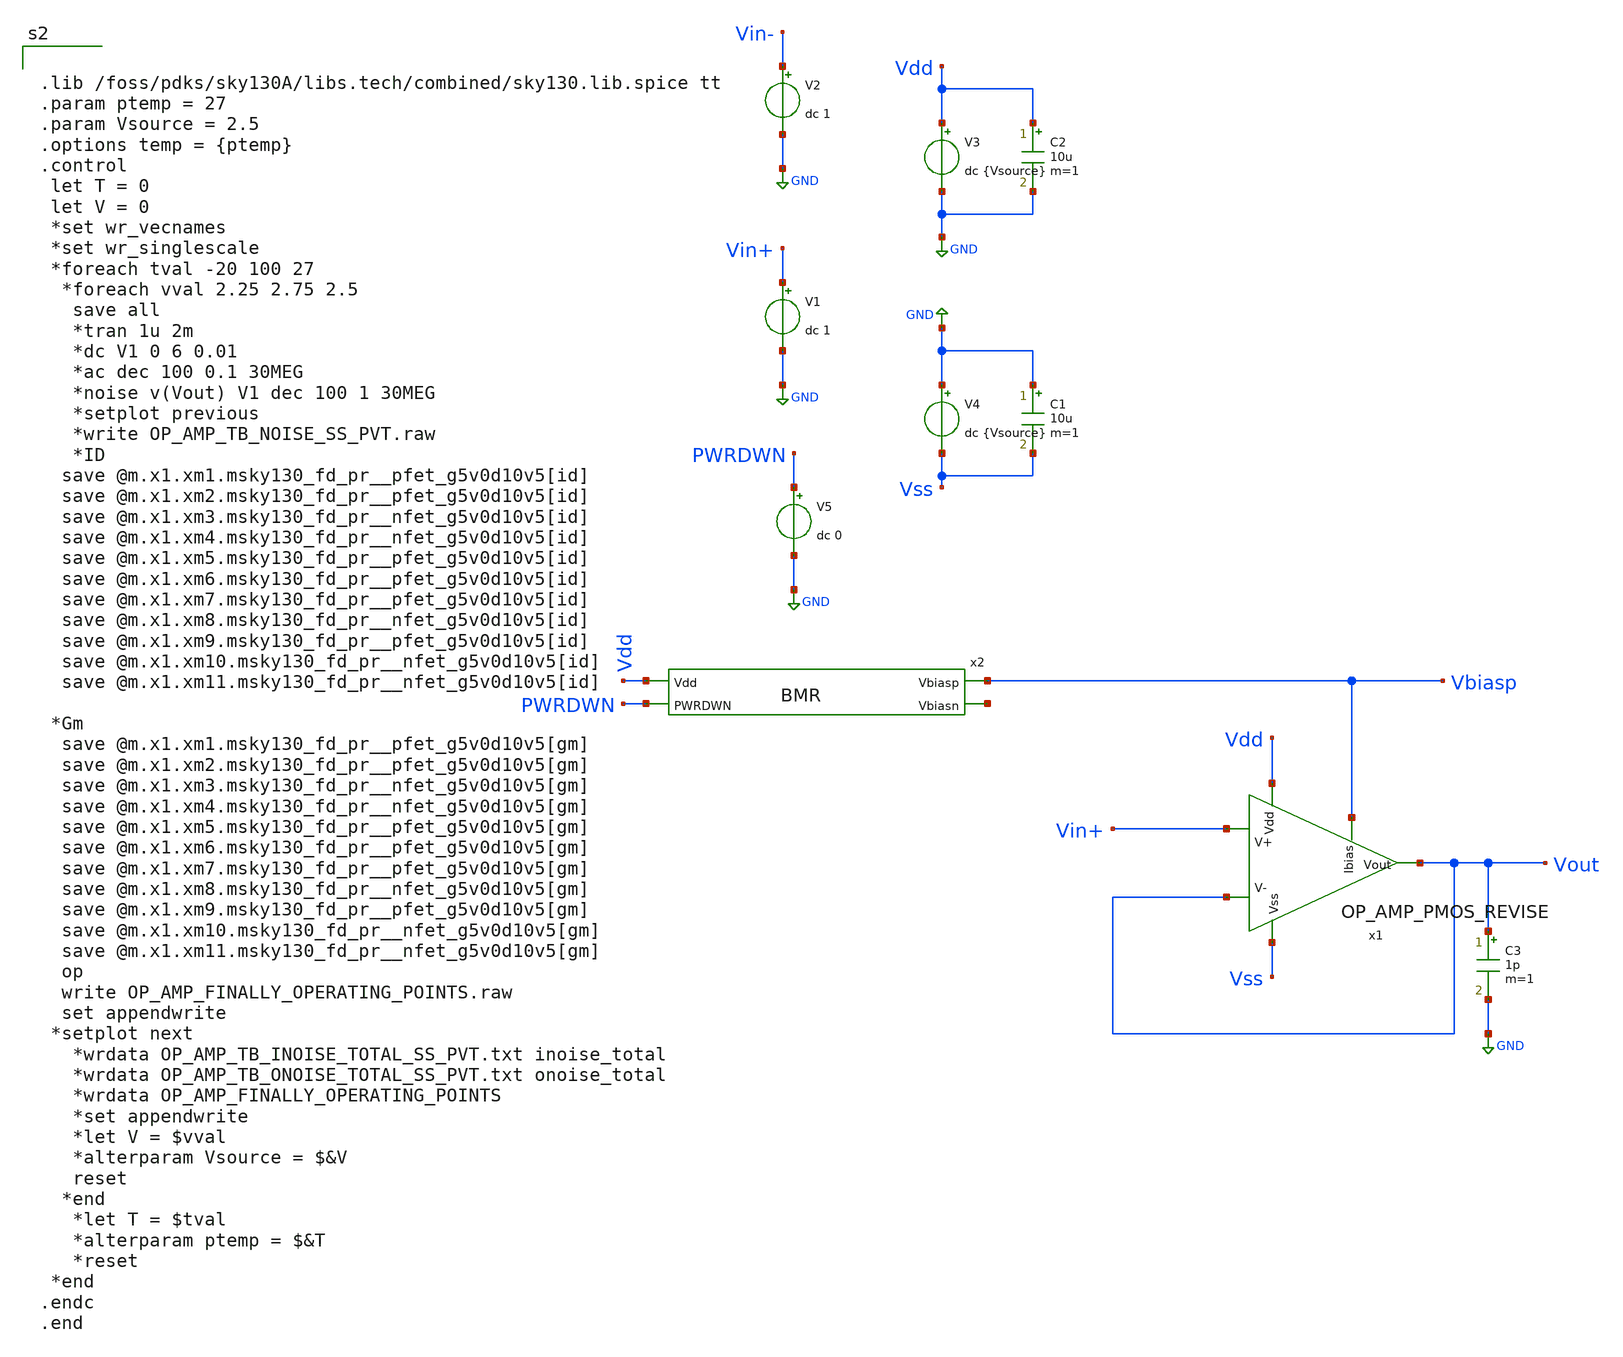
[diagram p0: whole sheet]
** sch_path: xschem/op_amp_tb_3.sch
**.subckt op_amp_tb_3
V1 Vin+ GND dc 1
V2 Vin- GND dc 1
V4 GND Vss dc {Vsource}
V3 Vdd GND dc {Vsource}
V5 PWRDWN GND dc 0
C1 GND Vss 10u m=1
C2 Vdd GND 10u m=1
x2 Vdd Vbiasp net1 PWRDWN BMR
x1 Vdd Vss Vbiasp Vout Vin+ Vout OP_AMP_PMOS_REVISE
C3 Vout GND 1p m=1
**** begin user architecture code


.lib /foss/pdks/sky130A/libs.tech/combined/sky130.lib.spice tt
.param ptemp = 27
.param Vsource = 2.5
.options temp = {ptemp}
.control
 let T = 0
 let V = 0
 *set wr_vecnames
 *set wr_singlescale
 *foreach tval -20 100 27
  *foreach vval 2.25 2.75 2.5
   save all
   *tran 1u 2m
   *dc V1 0 6 0.01
   *ac dec 100 0.1 30MEG
   *noise v(Vout) V1 dec 100 1 30MEG
   *setplot previous
   *write OP_AMP_TB_NOISE_SS_PVT.raw
   *ID
  save @m.x1.xm1.msky130_fd_pr__pfet_g5v0d10v5[id]
  save @m.x1.xm2.msky130_fd_pr__pfet_g5v0d10v5[id]
  save @m.x1.xm3.msky130_fd_pr__nfet_g5v0d10v5[id]
  save @m.x1.xm4.msky130_fd_pr__nfet_g5v0d10v5[id]
  save @m.x1.xm5.msky130_fd_pr__pfet_g5v0d10v5[id]
  save @m.x1.xm6.msky130_fd_pr__pfet_g5v0d10v5[id]
  save @m.x1.xm7.msky130_fd_pr__pfet_g5v0d10v5[id]
  save @m.x1.xm8.msky130_fd_pr__nfet_g5v0d10v5[id]
  save @m.x1.xm9.msky130_fd_pr__pfet_g5v0d10v5[id]
  save @m.x1.xm10.msky130_fd_pr__nfet_g5v0d10v5[id]
  save @m.x1.xm11.msky130_fd_pr__nfet_g5v0d10v5[id]

 *Gm
  save @m.x1.xm1.msky130_fd_pr__pfet_g5v0d10v5[gm]
  save @m.x1.xm2.msky130_fd_pr__pfet_g5v0d10v5[gm]
  save @m.x1.xm3.msky130_fd_pr__nfet_g5v0d10v5[gm]
  save @m.x1.xm4.msky130_fd_pr__nfet_g5v0d10v5[gm]
  save @m.x1.xm5.msky130_fd_pr__pfet_g5v0d10v5[gm]
  save @m.x1.xm6.msky130_fd_pr__pfet_g5v0d10v5[gm]
  save @m.x1.xm7.msky130_fd_pr__pfet_g5v0d10v5[gm]
  save @m.x1.xm8.msky130_fd_pr__nfet_g5v0d10v5[gm]
  save @m.x1.xm9.msky130_fd_pr__pfet_g5v0d10v5[gm]
  save @m.x1.xm10.msky130_fd_pr__nfet_g5v0d10v5[gm]
  save @m.x1.xm11.msky130_fd_pr__nfet_g5v0d10v5[gm]
  op
  write OP_AMP_FINALLY_OPERATING_POINTS.raw
  set appendwrite
 *setplot next
   *wrdata OP_AMP_TB_INOISE_TOTAL_SS_PVT.txt inoise_total
   *wrdata OP_AMP_TB_ONOISE_TOTAL_SS_PVT.txt onoise_total
   *wrdata OP_AMP_FINALLY_OPERATING_POINTS
   *set appendwrite
   *let V = $vval
   *alterparam Vsource = $&V
   reset
  *end
   *let T = $tval
   *alterparam ptemp = $&T
   *reset
 *end
.endc
.end

**** end user architecture code
**.ends

* expanding   symbol:  BMR.sym # of pins=4
** sym_path: xschem/BMR.sym
** sch_path: xschem/BMR.sch
.subckt BMR Vdd Vbiasp Vbiasn PWRDWN
*.ipin Vdd
*.opin Vbiasn
*.opin Vbiasp
*.ipin PWRDWN
XM3 Vbiasn Vbiasn GND GND sky130_fd_pr__nfet_g5v0d10v5 L=3 W=1.4 nf=1 ad='int((1 + 1)/2) * 1.4 / 1 * 0.29'
+ as='int((1 + 2)/2) * 1.4 / 1 * 0.29' pd='2*int((1 + 1)/2) * (1.4 / 1 + 0.29)' ps='2*int((1 + 2)/2) * (1.4 / 1 + 0.29)'
+ nrd='0.29 / 1.4 ' nrs='0.29 / 1.4 ' sa=0 sb=0 sd=0 mult=1 m=1
XM1 Vbiasp Vbiasp Vdd Vdd sky130_fd_pr__pfet_g5v0d10v5 L=3 W=31 nf=8 ad='int((8 + 1)/2) * 31 / 8 * 0.29'
+ as='int((8 + 2)/2) * 31 / 8 * 0.29' pd='2*int((8 + 1)/2) * (31 / 8 + 0.29)' ps='2*int((8 + 2)/2) * (31 / 8 + 0.29)'
+ nrd='0.29 / 31 ' nrs='0.29 / 31 ' sa=0 sb=0 sd=0 mult=2 m=2
XM2 Vbiasn Vbiasp Vdd Vdd sky130_fd_pr__pfet_g5v0d10v5 L=3 W=31 nf=8 ad='int((8 + 1)/2) * 31 / 8 * 0.29'
+ as='int((8 + 2)/2) * 31 / 8 * 0.29' pd='2*int((8 + 1)/2) * (31 / 8 + 0.29)' ps='2*int((8 + 2)/2) * (31 / 8 + 0.29)'
+ nrd='0.29 / 31 ' nrs='0.29 / 31 ' sa=0 sb=0 sd=0 mult=2 m=2
XM11 net1 PWRUP Vdd Vdd sky130_fd_pr__pfet_g5v0d10v5 L=10 W=1 nf=1 ad='int((1 + 1)/2) * 1 / 1 * 0.29'
+ as='int((1 + 2)/2) * 1 / 1 * 0.29' pd='2*int((1 + 1)/2) * (1 / 1 + 0.29)' ps='2*int((1 + 2)/2) * (1 / 1 + 0.29)'
+ nrd='0.29 / 1 ' nrs='0.29 / 1 ' sa=0 sb=0 sd=0 mult=1 m=1
XM4 Vbiasp Vbiasn net2 GND sky130_fd_pr__nfet_g5v0d10v5 L=3 W=1.4 nf=1 ad='int((1 + 1)/2) * 1.4 / 1 * 0.29'
+ as='int((1 + 2)/2) * 1.4 / 1 * 0.29' pd='2*int((1 + 1)/2) * (1.4 / 1 + 0.29)' ps='2*int((1 + 2)/2) * (1.4 / 1 + 0.29)'
+ nrd='0.29 / 1.4 ' nrs='0.29 / 1.4 ' sa=0 sb=0 sd=0 mult=2 m=2
XM5 net1 Vbiasn GND GND sky130_fd_pr__nfet_g5v0d10v5 L=3 W=1.4 nf=1 ad='int((1 + 1)/2) * 1.4 / 1 * 0.29'
+ as='int((1 + 2)/2) * 1.4 / 1 * 0.29' pd='2*int((1 + 1)/2) * (1.4 / 1 + 0.29)' ps='2*int((1 + 2)/2) * (1.4 / 1 + 0.29)'
+ nrd='0.29 / 1.4 ' nrs='0.29 / 1.4 ' sa=0 sb=0 sd=0 mult=1 m=1
XM7 net3 net1 Vbiasn GND sky130_fd_pr__nfet_g5v0d10v5 L=1 W=20 nf=1 ad='int((1 + 1)/2) * 20 / 1 * 0.29'
+ as='int((1 + 2)/2) * 20 / 1 * 0.29' pd='2*int((1 + 1)/2) * (20 / 1 + 0.29)' ps='2*int((1 + 2)/2) * (20 / 1 + 0.29)'
+ nrd='0.29 / 20 ' nrs='0.29 / 20 ' sa=0 sb=0 sd=0 mult=1 m=1
x1 Vdd PWRUP PWRDWN GND NOT_GATE
XM12 Vbiasp PWRUP net3 GND sky130_fd_pr__nfet_g5v0d10v5 L=1 W=20 nf=1 ad='int((1 + 1)/2) * 20 / 1 * 0.29'
+ as='int((1 + 2)/2) * 20 / 1 * 0.29' pd='2*int((1 + 1)/2) * (20 / 1 + 0.29)' ps='2*int((1 + 2)/2) * (20 / 1 + 0.29)'
+ nrd='0.29 / 20 ' nrs='0.29 / 20 ' sa=0 sb=0 sd=0 mult=1 m=1
XM9 Vbiasp PWRUP Vdd Vdd sky130_fd_pr__pfet_g5v0d10v5 L=1 W=3 nf=1 ad='int((1 + 1)/2) * 3 / 1 * 0.29'
+ as='int((1 + 2)/2) * 3 / 1 * 0.29' pd='2*int((1 + 1)/2) * (3 / 1 + 0.29)' ps='2*int((1 + 2)/2) * (3 / 1 + 0.29)'
+ nrd='0.29 / 3 ' nrs='0.29 / 3 ' sa=0 sb=0 sd=0 mult=1 m=1
XM10 Vbiasn PWRDWN GND GND sky130_fd_pr__nfet_g5v0d10v5 L=1 W=1 nf=1 ad='int((1 + 1)/2) * 1 / 1 * 0.29'
+ as='int((1 + 2)/2) * 1 / 1 * 0.29' pd='2*int((1 + 1)/2) * (1 / 1 + 0.29)' ps='2*int((1 + 2)/2) * (1 / 1 + 0.29)'
+ nrd='0.29 / 1 ' nrs='0.29 / 1 ' sa=0 sb=0 sd=0 mult=1 m=1
XR5 GND net2 GND sky130_fd_pr__res_xhigh_po_2p85 L=71.25 mult=1 m=1
XC10 Vdd net1 sky130_fd_pr__cap_mim_m3_1 W=10 L=10 MF=5 m=5
XC2 Vdd Vbiasp sky130_fd_pr__cap_mim_m3_1 W=10 L=10 MF=5 m=5
XC1 Vbiasn GND sky130_fd_pr__cap_mim_m3_1 W=10 L=10 MF=5 m=5
.ends


* expanding   symbol:  OP_AMP_PMOS_REVISE.sym # of pins=6
** sym_path: xschem/OP_AMP_PMOS_REVISE.sym
** sch_path: xschem/OP_AMP_PMOS_REVISE.sch
.subckt OP_AMP_PMOS_REVISE Vdd Vss Ibias Vout V+ V-
*.ipin V-
*.ipin V+
*.ipin Vdd
*.ipin Vss
*.ipin Ibias
*.opin Vout
XM3 net2 net1 Vss Vss sky130_fd_pr__nfet_g5v0d10v5 L=6 W=0.81 nf=1 ad='int((1 + 1)/2) * 0.81 / 1 * 0.29'
+ as='int((1 + 2)/2) * 0.81 / 1 * 0.29' pd='2*int((1 + 1)/2) * (0.81 / 1 + 0.29)' ps='2*int((1 + 2)/2) * (0.81 / 1 + 0.29)'
+ nrd='0.29 / 0.81 ' nrs='0.29 / 0.81 ' sa=0 sb=0 sd=0 mult=2 m=2
XM1 net2 V+ net3 net3 sky130_fd_pr__pfet_g5v0d10v5 L=3 W=80 nf=8 ad='int((8 + 1)/2) * 80 / 8 * 0.29'
+ as='int((8 + 2)/2) * 80 / 8 * 0.29' pd='2*int((8 + 1)/2) * (80 / 8 + 0.29)' ps='2*int((8 + 2)/2) * (80 / 8 + 0.29)'
+ nrd='0.29 / 80 ' nrs='0.29 / 80 ' sa=0 sb=0 sd=0 mult=4 m=4
XM2 net1 V- net3 net3 sky130_fd_pr__pfet_g5v0d10v5 L=3 W=80 nf=8 ad='int((8 + 1)/2) * 80 / 8 * 0.29'
+ as='int((8 + 2)/2) * 80 / 8 * 0.29' pd='2*int((8 + 1)/2) * (80 / 8 + 0.29)' ps='2*int((8 + 2)/2) * (80 / 8 + 0.29)'
+ nrd='0.29 / 80 ' nrs='0.29 / 80 ' sa=0 sb=0 sd=0 mult=4 m=4
XM4 net1 net1 Vss Vss sky130_fd_pr__nfet_g5v0d10v5 L=6 W=0.81 nf=1 ad='int((1 + 1)/2) * 0.81 / 1 * 0.29'
+ as='int((1 + 2)/2) * 0.81 / 1 * 0.29' pd='2*int((1 + 1)/2) * (0.81 / 1 + 0.29)' ps='2*int((1 + 2)/2) * (0.81 / 1 + 0.29)'
+ nrd='0.29 / 0.81 ' nrs='0.29 / 0.81 ' sa=0 sb=0 sd=0 mult=2 m=2
XM8 net4 net2 Vss Vss sky130_fd_pr__nfet_g5v0d10v5 L=3 W=14 nf=4 ad='int((4 + 1)/2) * 14 / 4 * 0.29'
+ as='int((4 + 2)/2) * 14 / 4 * 0.29' pd='2*int((4 + 1)/2) * (14 / 4 + 0.29)' ps='2*int((4 + 2)/2) * (14 / 4 + 0.29)'
+ nrd='0.29 / 14 ' nrs='0.29 / 14 ' sa=0 sb=0 sd=0 mult=2 m=2
XM5 net3 Ibias Vdd Vdd sky130_fd_pr__pfet_g5v0d10v5 L=3 W=31 nf=8 ad='int((8 + 1)/2) * 31 / 8 * 0.29'
+ as='int((8 + 2)/2) * 31 / 8 * 0.29' pd='2*int((8 + 1)/2) * (31 / 8 + 0.29)' ps='2*int((8 + 2)/2) * (31 / 8 + 0.29)'
+ nrd='0.29 / 31 ' nrs='0.29 / 31 ' sa=0 sb=0 sd=0 mult=2 m=2
XM6 net6 Ibias Vdd Vdd sky130_fd_pr__pfet_g5v0d10v5 L=3 W=31 nf=8 ad='int((8 + 1)/2) * 31 / 8 * 0.29'
+ as='int((8 + 2)/2) * 31 / 8 * 0.29' pd='2*int((8 + 1)/2) * (31 / 8 + 0.29)' ps='2*int((8 + 2)/2) * (31 / 8 + 0.29)'
+ nrd='0.29 / 31 ' nrs='0.29 / 31 ' sa=0 sb=0 sd=0 mult=30 m=30
XM7 net4 net4 net5 net5 sky130_fd_pr__pfet_g5v0d10v5 L=3 W=41.1 nf=4 ad='int((4 + 1)/2) * 41.1 / 4 * 0.29'
+ as='int((4 + 2)/2) * 41.1 / 4 * 0.29' pd='2*int((4 + 1)/2) * (41.1 / 4 + 0.29)' ps='2*int((4 + 2)/2) * (41.1 / 4 + 0.29)'
+ nrd='0.29 / 41.1 ' nrs='0.29 / 41.1 ' sa=0 sb=0 sd=0 mult=4 m=4
XM9 Vss net4 Vout Vout sky130_fd_pr__pfet_g5v0d10v5 L=3 W=41.1 nf=4 ad='int((4 + 1)/2) * 41.1 / 4 * 0.29'
+ as='int((4 + 2)/2) * 41.1 / 4 * 0.29' pd='2*int((4 + 1)/2) * (41.1 / 4 + 0.29)' ps='2*int((4 + 2)/2) * (41.1 / 4 + 0.29)'
+ nrd='0.29 / 41.1 ' nrs='0.29 / 41.1 ' sa=0 sb=0 sd=0 mult=4 m=4
XM10 net6 net6 net5 net5 sky130_fd_pr__nfet_g5v0d10v5 L=3 W=18 nf=4 ad='int((4 + 1)/2) * 18 / 4 * 0.29'
+ as='int((4 + 2)/2) * 18 / 4 * 0.29' pd='2*int((4 + 1)/2) * (18 / 4 + 0.29)' ps='2*int((4 + 2)/2) * (18 / 4 + 0.29)'
+ nrd='0.29 / 18 ' nrs='0.29 / 18 ' sa=0 sb=0 sd=0 mult=2 m=2
XM11 Vdd net6 Vout Vout sky130_fd_pr__nfet_g5v0d10v5 L=3 W=18 nf=4 ad='int((4 + 1)/2) * 18 / 4 * 0.29'
+ as='int((4 + 2)/2) * 18 / 4 * 0.29' pd='2*int((4 + 1)/2) * (18 / 4 + 0.29)' ps='2*int((4 + 2)/2) * (18 / 4 + 0.29)'
+ nrd='0.29 / 18 ' nrs='0.29 / 18 ' sa=0 sb=0 sd=0 mult=2 m=2
XC10 net2 net4 sky130_fd_pr__cap_mim_m3_1 W=10 L=10 MF=5 m=5
.ends


* expanding   symbol:  NOT_GATE.sym # of pins=4
** sym_path: xschem/NOT_GATE.sym
** sch_path: xschem/NOT_GATE.sch
.subckt NOT_GATE Vdd Vout Vin Vss
*.opin Vout
*.ipin Vdd
*.ipin Vss
*.ipin Vin
XM1 Vout Vin Vss Vss sky130_fd_pr__nfet_g5v0d10v5 L=1 W=1 nf=1 ad='int((1 + 1)/2) * 1 / 1 * 0.29' as='int((1 + 2)/2) * 1 / 1 * 0.29'
+ pd='2*int((1 + 1)/2) * (1 / 1 + 0.29)' ps='2*int((1 + 2)/2) * (1 / 1 + 0.29)' nrd='0.29 / 1 ' nrs='0.29 / 1 '
+ sa=0 sb=0 sd=0 mult=1 m=1
XM2 Vout Vin Vdd Vdd sky130_fd_pr__pfet_g5v0d10v5 L=1 W=3 nf=1 ad='int((1 + 1)/2) * 3 / 1 * 0.29' as='int((1 + 2)/2) * 3 / 1 * 0.29'
+ pd='2*int((1 + 1)/2) * (3 / 1 + 0.29)' ps='2*int((1 + 2)/2) * (3 / 1 + 0.29)' nrd='0.29 / 3 ' nrs='0.29 / 3 '
+ sa=0 sb=0 sd=0 mult=1 m=1
.ends

.GLOBAL GND
.end
